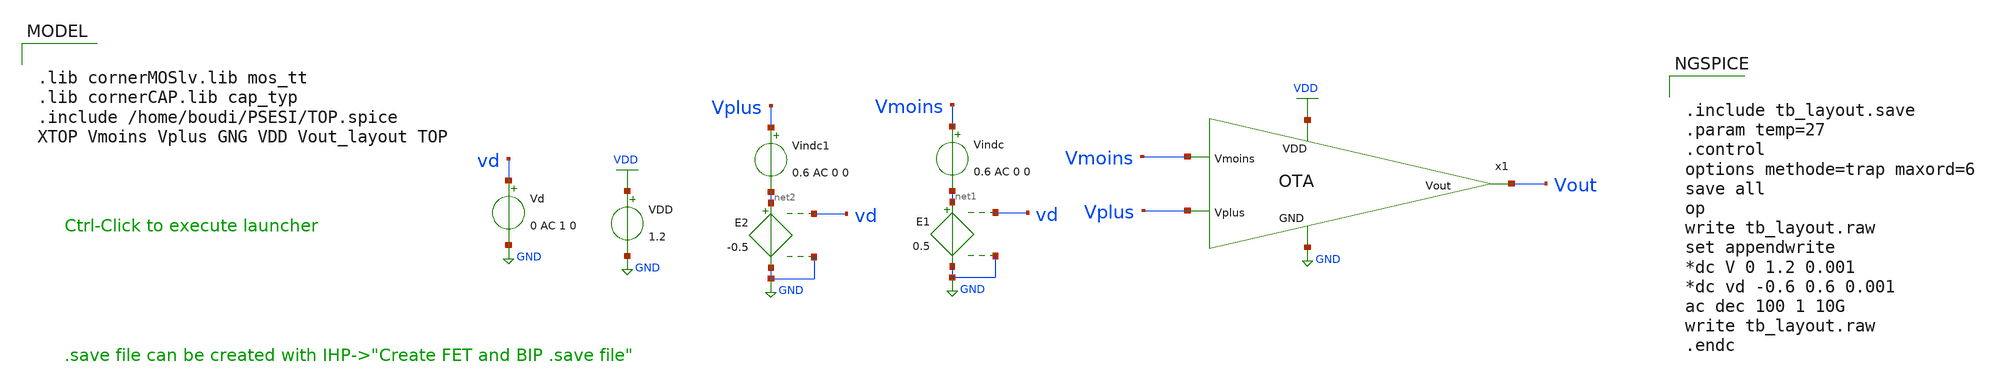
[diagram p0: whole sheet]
** sch_path: tb_layout.sch
**.subckt tb_layout
Vindc Vmoins net1 0.6 AC 0 0
Vd vd GND 0 AC 1 0
E1 net1 GND vd GND 0.5
Vindc1 Vplus net2 0.6 AC 0 0
E2 net2 GND vd GND -0.5
VDD VDD GND 1.2
x1 VDD Vmoins Vplus Vout GND OTA
**** begin user architecture code

.lib cornerMOSlv.lib mos_tt
.lib cornerCAP.lib cap_typ
.include /home/boudi/PSESI/TOP.spice
XTOP Vmoins Vplus GNG VDD Vout_layout TOP



.include tb_layout.save
.param temp=27
.control
options methode=trap maxord=6
save all
op
write tb_layout.raw
set appendwrite
*dc V 0 1.2 0.001
*dc vd -0.6 0.6 0.001
ac dec 100 1 10G
write tb_layout.raw
.endc


**** end user architecture code
**.ends

* expanding   symbol:  OTA.sym # of pins=5
** sym_path: OTA.sym
** sch_path: OTA.sch
.subckt OTA VDD Vmoins Vplus Vout GND
*.ipin Vmoins
*.ipin Vplus
*.ipin VDD
*.ipin GND
*.opin Vout
XM3 net1 net4 GND GND sg13_lv_nmos w=2.5u l=0.5u ng=1 m=1 mm_ok=1
XM2.1 net2 Vmoins net1 GND sg13_lv_nmos w=2.5u l=0.5u ng=2 m=1 mm_ok=1
XM2.2 net3 Vplus net1 GND sg13_lv_nmos w=2.5u l=0.5u ng=2 m=1 mm_ok=1
XM1.1 net2 net2 VDD VDD sg13_lv_pmos w=2.5u l=0.5u ng=1 m=1 mm_ok=1
XM1.2 net3 net2 VDD VDD sg13_lv_pmos w=2.5u l=0.5u ng=1 m=1 mm_ok=1
XM4 Vout net4 GND GND sg13_lv_nmos w=3.0u l=1.6u ng=2 m=1 mm_ok=1
XM5 Vout net3 VDD VDD sg13_lv_pmos w=4.0u l=0.5u ng=2 m=1 mm_ok=1
XC2 net3 Vout cap_cmim w=10.0e-6 l=10.0e-6 m=1 mm_ok=1
XM1 net4 net4 GND GND sg13_lv_nmos w=8.0u l=0.5u ng=4 m=1 mm_ok=1
XM2 net4 net4 VDD VDD sg13_lv_pmos w=1.8u l=0.5u ng=1 m=1 mm_ok=1
.ends

.GLOBAL GND
.GLOBAL VDD
.end
